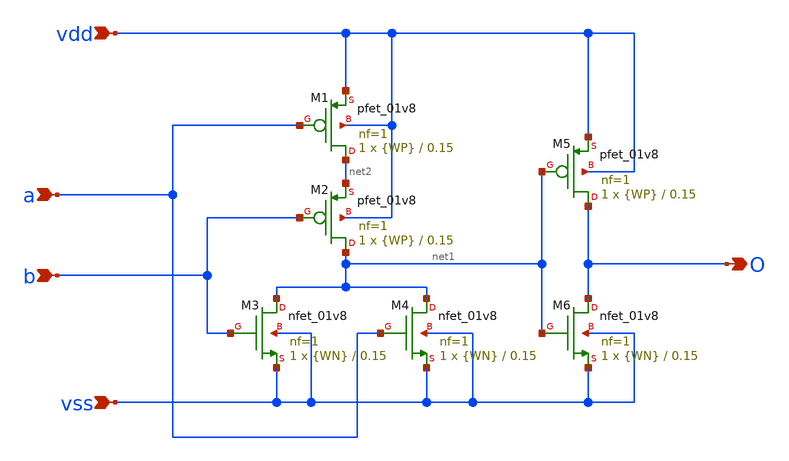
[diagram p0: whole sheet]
** sch_path: eamta2021/sch/or/or.sch
**.subckt or vdd a b vss O
*.ipin vdd
*.ipin a
*.ipin b
*.ipin vss
*.opin O
XM1 net2 a vdd vdd sky130_fd_pr__pfet_01v8 L=0.15 W={WP} nf=1 ad='int((nf+1)/2) * W/nf * 0.29' as='int((nf+2)/2) * W/nf * 0.29'
+ pd='2*int((nf+1)/2) * (W/nf + 0.29)' ps='2*int((nf+2)/2) * (W/nf + 0.29)' nrd='0.29 / W' nrs='0.29 / W'
+ sa=0 sb=0 sd=0 mult=1 m=1
XM2 net1 b net2 vdd sky130_fd_pr__pfet_01v8 L=0.15 W={WP} nf=1 ad='int((nf+1)/2) * W/nf * 0.29' as='int((nf+2)/2) * W/nf * 0.29'
+ pd='2*int((nf+1)/2) * (W/nf + 0.29)' ps='2*int((nf+2)/2) * (W/nf + 0.29)' nrd='0.29 / W' nrs='0.29 / W'
+ sa=0 sb=0 sd=0 mult=1 m=1
XM3 net1 b vss vss sky130_fd_pr__nfet_01v8 L=0.15 W={WN} nf=1 ad='int((nf+1)/2) * W/nf * 0.29' as='int((nf+2)/2) * W/nf * 0.29'
+ pd='2*int((nf+1)/2) * (W/nf + 0.29)' ps='2*int((nf+2)/2) * (W/nf + 0.29)' nrd='0.29 / W' nrs='0.29 / W'
+ sa=0 sb=0 sd=0 mult=1 m=1
XM4 net1 a vss vss sky130_fd_pr__nfet_01v8 L=0.15 W={WN} nf=1 ad='int((nf+1)/2) * W/nf * 0.29' as='int((nf+2)/2) * W/nf * 0.29'
+ pd='2*int((nf+1)/2) * (W/nf + 0.29)' ps='2*int((nf+2)/2) * (W/nf + 0.29)' nrd='0.29 / W' nrs='0.29 / W'
+ sa=0 sb=0 sd=0 mult=1 m=1
XM5 O net1 vdd vdd sky130_fd_pr__pfet_01v8 L=0.15 W={WP} nf=1 ad='int((nf+1)/2) * W/nf * 0.29' as='int((nf+2)/2) * W/nf * 0.29'
+ pd='2*int((nf+1)/2) * (W/nf + 0.29)' ps='2*int((nf+2)/2) * (W/nf + 0.29)' nrd='0.29 / W' nrs='0.29 / W'
+ sa=0 sb=0 sd=0 mult=1 m=1
XM6 O net1 vss vss sky130_fd_pr__nfet_01v8 L=0.15 W={WN} nf=1 ad='int((nf+1)/2) * W/nf * 0.29' as='int((nf+2)/2) * W/nf * 0.29'
+ pd='2*int((nf+1)/2) * (W/nf + 0.29)' ps='2*int((nf+2)/2) * (W/nf + 0.29)' nrd='0.29 / W' nrs='0.29 / W'
+ sa=0 sb=0 sd=0 mult=1 m=1
**.ends
.end
